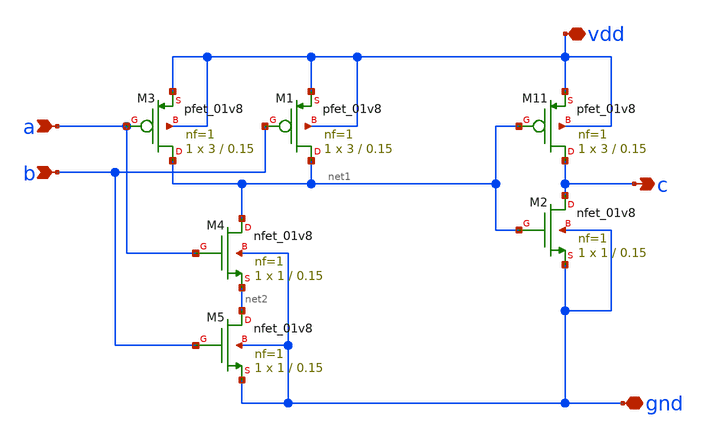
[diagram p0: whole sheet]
** sch_path: and.sch
**.subckt and vdd gnd a c b
*.iopin vdd
*.iopin gnd
*.ipin a
*.opin c
*.ipin b
XM2 c net1 gnd gnd sky130_fd_pr__nfet_01v8 L=0.15 W=1 nf=1 ad='int((1 + 1)/2) * 1 / 1 * 0.29' as='int((1 + 2)/2) * 1 / 1 * 0.29'
+ pd='2*int((1 + 1)/2) * (1 / 1 + 0.29)' ps='2*int((1 + 2)/2) * (1 / 1 + 0.29)' nrd='0.29 / 1 ' nrs='0.29 / 1 '
+ sa=0 sb=0 sd=0 mult=1 m=1
XM11 c net1 vdd vdd sky130_fd_pr__pfet_01v8 L=0.15 W=3 nf=1 ad='int((nf+1)/2) * W/nf * 0.29' as='int((nf+2)/2) * W/nf * 0.29'
+ pd='2*int((nf+1)/2) * (W/nf + 0.29)' ps='2*int((nf+2)/2) * (W/nf + 0.29)' nrd='0.29 / W' nrs='0.29 / W'
+ sa=0 sb=0 sd=0 mult=1 m=1
XM1 net1 b vdd vdd sky130_fd_pr__pfet_01v8 L=0.15 W=3 nf=1 ad='int((nf+1)/2) * W/nf * 0.29' as='int((nf+2)/2) * W/nf * 0.29'
+ pd='2*int((nf+1)/2) * (W/nf + 0.29)' ps='2*int((nf+2)/2) * (W/nf + 0.29)' nrd='0.29 / W' nrs='0.29 / W'
+ sa=0 sb=0 sd=0 mult=1 m=1
XM3 net1 a vdd vdd sky130_fd_pr__pfet_01v8 L=0.15 W=3 nf=1 ad='int((nf+1)/2) * W/nf * 0.29' as='int((nf+2)/2) * W/nf * 0.29'
+ pd='2*int((nf+1)/2) * (W/nf + 0.29)' ps='2*int((nf+2)/2) * (W/nf + 0.29)' nrd='0.29 / W' nrs='0.29 / W'
+ sa=0 sb=0 sd=0 mult=1 m=1
XM4 net1 a net2 gnd sky130_fd_pr__nfet_01v8 L=0.15 W=1 nf=1 ad='int((1 + 1)/2) * 1 / 1 * 0.29' as='int((1 + 2)/2) * 1 / 1 * 0.29'
+ pd='2*int((1 + 1)/2) * (1 / 1 + 0.29)' ps='2*int((1 + 2)/2) * (1 / 1 + 0.29)' nrd='0.29 / 1 ' nrs='0.29 / 1 '
+ sa=0 sb=0 sd=0 mult=1 m=1
XM5 net2 b gnd gnd sky130_fd_pr__nfet_01v8 L=0.15 W=1 nf=1 ad='int((1 + 1)/2) * 1 / 1 * 0.29' as='int((1 + 2)/2) * 1 / 1 * 0.29'
+ pd='2*int((1 + 1)/2) * (1 / 1 + 0.29)' ps='2*int((1 + 2)/2) * (1 / 1 + 0.29)' nrd='0.29 / 1 ' nrs='0.29 / 1 '
+ sa=0 sb=0 sd=0 mult=1 m=1
**.ends
.end
